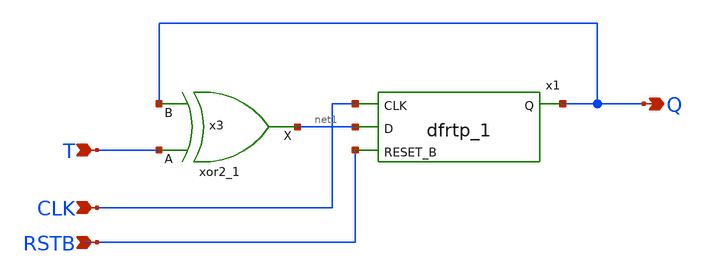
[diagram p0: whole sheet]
** sch_path: xschem/T_flip_flop/asyn_rst_t_ff.sch
**.subckt asyn_rst_t_ff T CLK Q RSTB
*.ipin T
*.ipin CLK
*.opin Q
*.ipin RSTB
x1 CLK net1 RSTB GND GND VDD VDD Q sky130_fd_sc_lp__dfrtp_1
x3 T Q GND GND VDD VDD net1 sky130_fd_sc_lp__xor2_1
**.ends
.end
